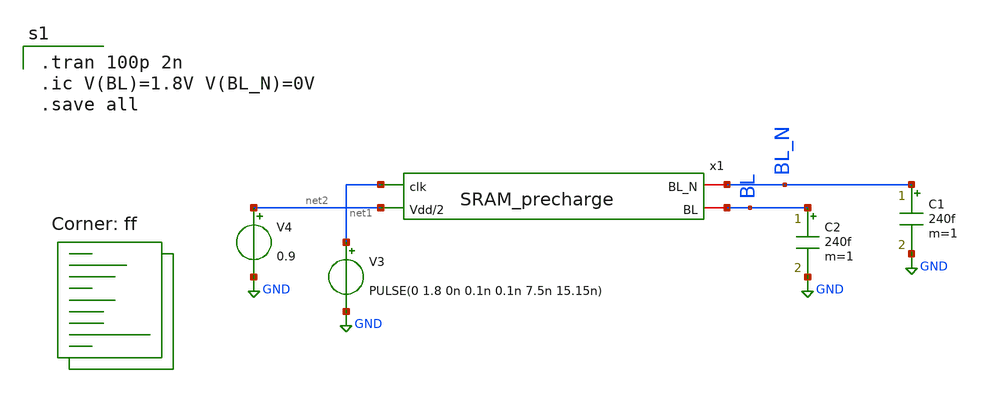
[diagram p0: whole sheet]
** sch_path: analog/schematics/tb.sch
**.subckt tb
x1 BL_N BL net1 net2 SRAM_precharge
C1 BL_N GND 240f m=1
C2 BL GND 240f m=1
V3 net1 GND PULSE(0 1.8 0n 0.1n 0.1n 7.5n 15.15n)
V4 net2 GND 0.9
**** begin user architecture code

.tran 100p 2n
.ic V(BL)=1.8V V(BL_N)=0V
.save all

.lib $::SKYWATER_MODELS/sky130.lib.spice ff
**** end user architecture code
**.ends
.GLOBAL GND
.end
